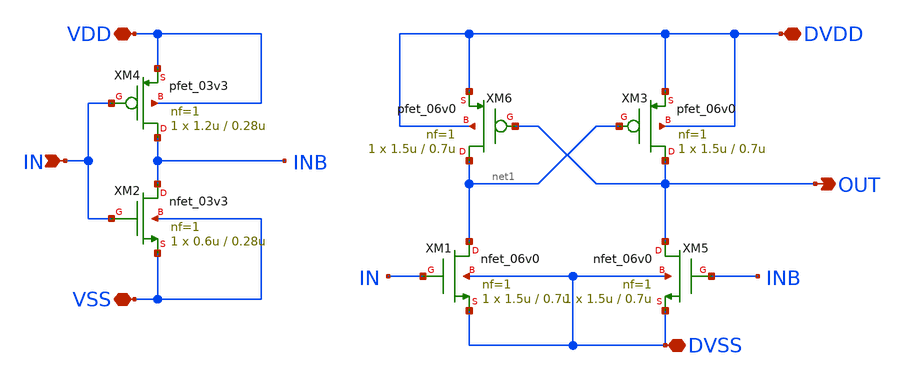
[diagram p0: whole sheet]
** sch_path: xschem/io_lvlshft.sch
* Copyright 2023 David Mitchell Bailey
* Licensed under the Apache License, Version 2.0 (the "License");
* you may not use this file except in compliance with the License.
* You may obtain a copy of the License at
* https://www.apache.org/licenses/LICENSE-2.0
* Unless required by applicable law or agreed to in writing, software
* distributed under the License is distributed on an "AS IS" BASIS,
* WITHOUT WARRANTIES OR CONDITIONS OF ANY KIND, either express or implied.
* See the License for the specific language governing permissions and
* limitations under the License.
**.subckt io_lvlshft OUT IN VDD VSS DVSS DVDD
*.opin OUT
*.ipin IN
*.iopin VDD
*.iopin VSS
*.iopin DVSS
*.iopin DVDD
XM2 INB IN VSS VSS nfet_03v3 L=0.28u W=0.6u nf=1 ad='int((nf+1)/2) * W/nf * 0.18u' as='int((nf+2)/2) * W/nf * 0.18u'
+ pd='2*int((nf+1)/2) * (W/nf + 0.18u)' ps='2*int((nf+2)/2) * (W/nf + 0.18u)' nrd='0.18u / W' nrs='0.18u / W'
+ sa=0 sb=0 sd=0 m=1 par=1
XM4 INB IN VDD VDD pfet_03v3 L=0.28u W=1.2u nf=1 ad='int((nf+1)/2) * W/nf * 0.18u' as='int((nf+2)/2) * W/nf * 0.18u'
+ pd='2*int((nf+1)/2) * (W/nf + 0.18u)' ps='2*int((nf+2)/2) * (W/nf + 0.18u)' nrd='0.18u / W' nrs='0.18u / W'
+ sa=0 sb=0 sd=0 m=1 par=1
XM1 net1 IN DVSS DVSS nfet_06v0 L=0.7u W=1.5u nf=1 ad='int((nf+1)/2) * W/nf * 0.18u' as='int((nf+2)/2) * W/nf * 0.18u'
+ pd='2*int((nf+1)/2) * (W/nf + 0.18u)' ps='2*int((nf+2)/2) * (W/nf + 0.18u)' nrd='0.18u / W' nrs='0.18u / W'
+ sa=0 sb=0 sd=0 m=1 par=1
XM3 OUT net1 DVDD DVDD pfet_06v0 L=0.7u W=1.5u nf=1 ad='int((nf+1)/2) * W/nf * 0.18u' as='int((nf+2)/2) * W/nf * 0.18u'
+ pd='2*int((nf+1)/2) * (W/nf + 0.18u)' ps='2*int((nf+2)/2) * (W/nf + 0.18u)' nrd='0.18u / W' nrs='0.18u / W'
+ sa=0 sb=0 sd=0 m=1
XM5 OUT INB DVSS DVSS nfet_06v0 L=0.7u W=1.5u nf=1 ad='int((nf+1)/2) * W/nf * 0.18u' as='int((nf+2)/2) * W/nf * 0.18u'
+ pd='2*int((nf+1)/2) * (W/nf + 0.18u)' ps='2*int((nf+2)/2) * (W/nf + 0.18u)' nrd='0.18u / W' nrs='0.18u / W'
+ sa=0 sb=0 sd=0 m=1 par=1
XM6 net1 OUT DVDD DVDD pfet_06v0 L=0.7u W=1.5u nf=1 ad='int((nf+1)/2) * W/nf * 0.18u' as='int((nf+2)/2) * W/nf * 0.18u'
+ pd='2*int((nf+1)/2) * (W/nf + 0.18u)' ps='2*int((nf+2)/2) * (W/nf + 0.18u)' nrd='0.18u / W' nrs='0.18u / W'
+ sa=0 sb=0 sd=0 m=1
**.ends
.end
